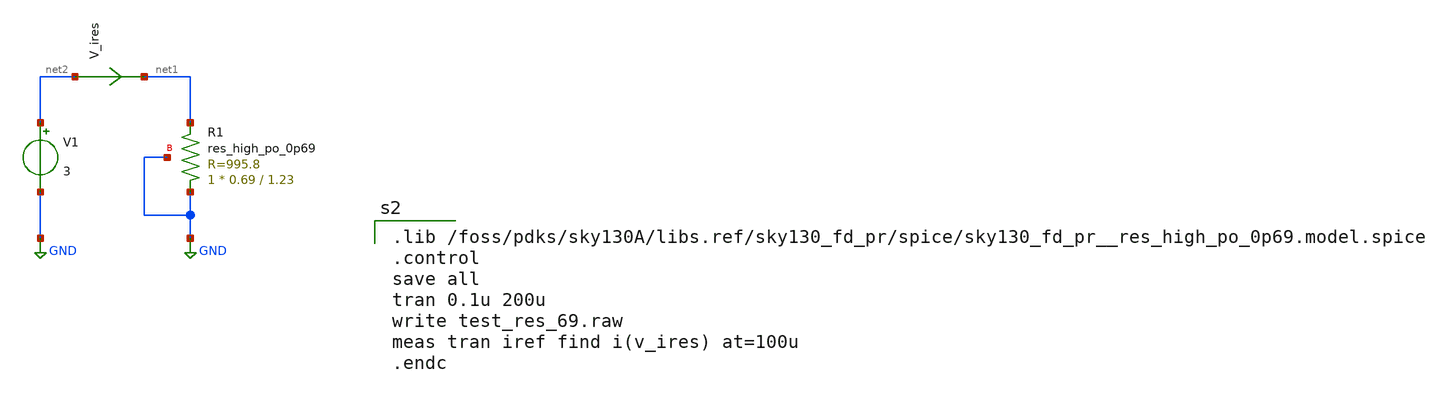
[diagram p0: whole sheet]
** sch_path: xschem/test_res_69.sch
**.subckt test_res_69
XR1 GND net1 GND sky130_fd_pr__res_high_po_0p69 L=1.23 mult=1 m=1
V1 net2 GND 3
V_ires net2 net1 0
.save i(v_ires)
**** begin user architecture code

.lib /foss/pdks/sky130A/libs.ref/sky130_fd_pr/spice/sky130_fd_pr__res_high_po_0p69.model.spice
.control
save all
tran 0.1u 200u
write test_res_69.raw
meas tran iref find i(v_ires) at=100u
.endc


** opencircuitdesign pdks install
.lib $::SKYWATER_MODELS/sky130.lib.spice tt


**** end user architecture code
**.ends
.GLOBAL GND
.end
